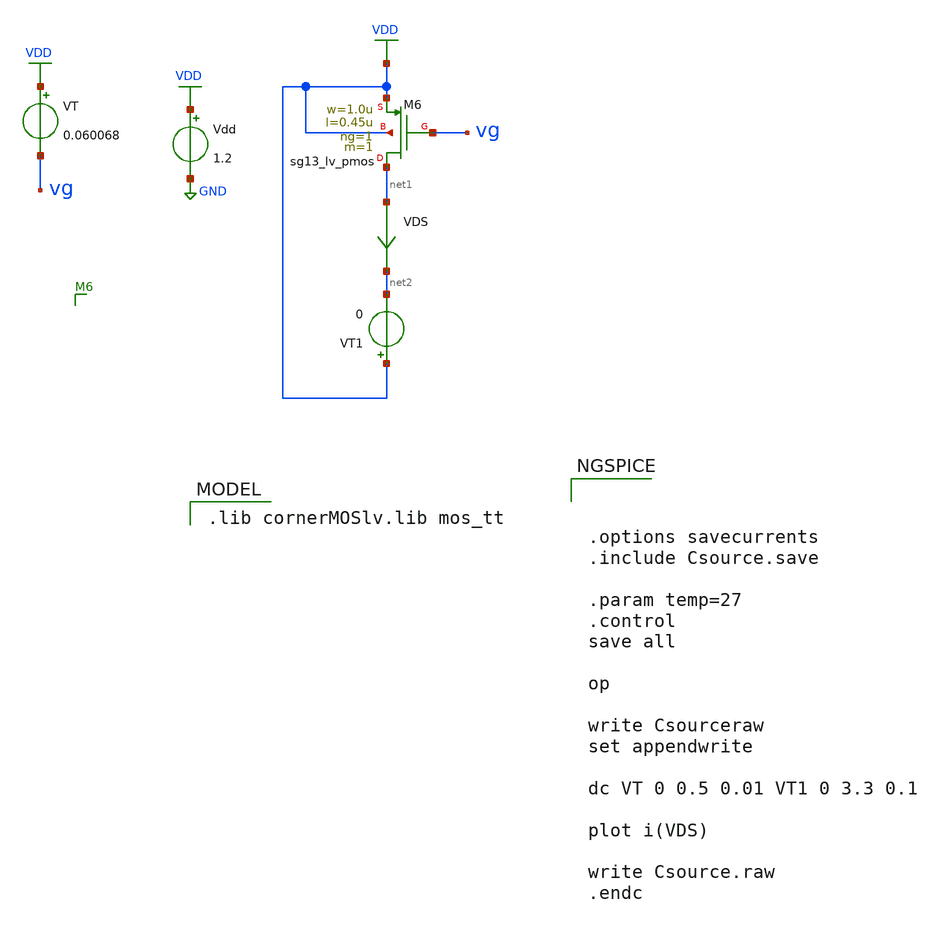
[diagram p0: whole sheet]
** sch_path: blocks/composite/dpi_adexp_neuron/design_data/xschem/legacy/Csource2.sch
**.subckt Csource2
XM6 net1 vg VDD VDD sg13_lv_pmos w=1.0u l=0.45u ng=1 m=1 mm_ok=1
Vdd VDD GND 1.2
VDS net1 net2 0
.save i(vds)
VT VDD vg 0.060068
VT1 VDD net2 0
**** begin user architecture code



.options savecurrents
.include Csource.save

.param temp=27
.control
save all

op

write Csourceraw
set appendwrite

dc VT 0 0.5 0.01 VT1 0 3.3 0.1

plot i(VDS)

write Csource.raw
.endc


 .lib cornerMOSlv.lib mos_tt

**** end user architecture code
**.ends
.GLOBAL VDD
.GLOBAL GND
.end
